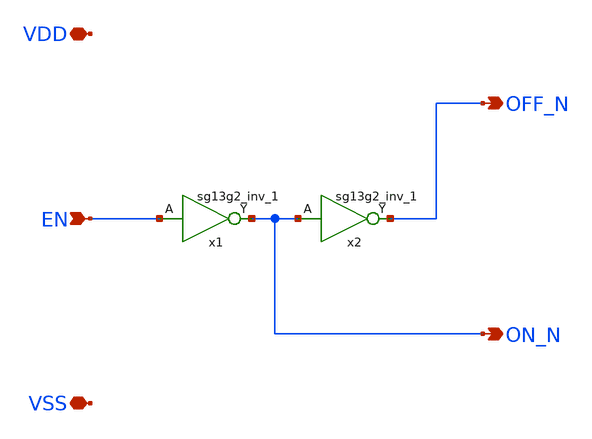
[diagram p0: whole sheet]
** sch_path: xschem/switch_logic.sch
**.subckt switch_logic VSS VDD EN OFF_N ON_N
*.iopin VSS
*.iopin VDD
*.ipin EN
*.opin OFF_N
*.opin ON_N
x1 ON_N EN VDD VSS sg13g2_inv_1
x2 OFF_N ON_N VDD VSS sg13g2_inv_1
**.ends

* expanding   symbol:  sg13g2_stdcells/sg13g2_inv_1.sym # of pins=2
** sym_path: sg13g2_stdcells/sg13g2_inv_1.sym
** sch_path: sg13g2_stdcells/sg13g2_inv_1.sch
.subckt sg13g2_inv_1 Y A VDD VSS
*.opin Y
*.ipin A
*.iopin VDD
*.iopin VSS
XM1 Y A VSS VSS sg13_lv_nmos w=740.00n l=130.00n ng=1 m=1 mm_ok=1
XM2 Y A VDD VDD sg13_lv_pmos w=1.12u l=130.00n ng=1 m=1 mm_ok=1
.ends

.end
